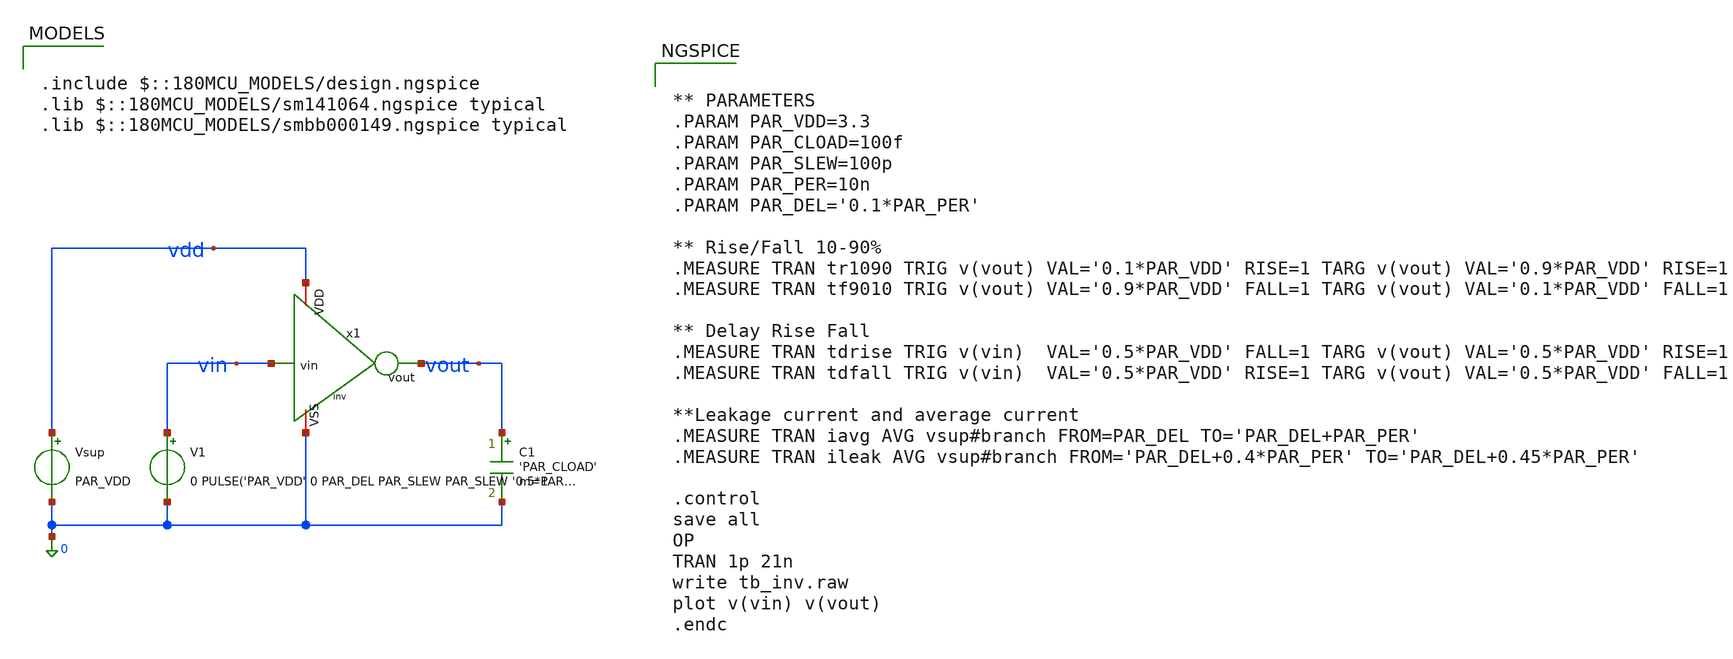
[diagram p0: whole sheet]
** sch_path: sar_logic/sar_designs/tb_inv.sch
**.subckt tb_inv
V1 vin 0 0 PULSE('PAR_VDD' 0 PAR_DEL PAR_SLEW PAR_SLEW '0.5*PAR_PER' '1.0*PAR_PER')
Vsup vdd 0 PAR_VDD
C1 vout 0 'PAR_CLOAD' m=1
x1 vdd vin vout 0 inv
**** begin user architecture code

.include $::180MCU_MODELS/design.ngspice
.lib $::180MCU_MODELS/sm141064.ngspice typical
.lib $::180MCU_MODELS/smbb000149.ngspice typical



** PARAMETERS
.PARAM PAR_VDD=3.3
.PARAM PAR_CLOAD=100f
.PARAM PAR_SLEW=100p
.PARAM PAR_PER=10n
.PARAM PAR_DEL='0.1*PAR_PER'

** Rise/Fall 10-90%
.MEASURE TRAN tr1090 TRIG v(vout) VAL='0.1*PAR_VDD' RISE=1 TARG v(vout) VAL='0.9*PAR_VDD' RISE=1
.MEASURE TRAN tf9010 TRIG v(vout) VAL='0.9*PAR_VDD' FALL=1 TARG v(vout) VAL='0.1*PAR_VDD' FALL=1

** Delay Rise Fall
.MEASURE TRAN tdrise TRIG v(vin)  VAL='0.5*PAR_VDD' FALL=1 TARG v(vout) VAL='0.5*PAR_VDD' RISE=1
.MEASURE TRAN tdfall TRIG v(vin)  VAL='0.5*PAR_VDD' RISE=1 TARG v(vout) VAL='0.5*PAR_VDD' FALL=1

**Leakage current and average current
.MEASURE TRAN iavg AVG vsup#branch FROM=PAR_DEL TO='PAR_DEL+PAR_PER'
.MEASURE TRAN ileak AVG vsup#branch FROM='PAR_DEL+0.4*PAR_PER' TO='PAR_DEL+0.45*PAR_PER'

.control
save all
OP
TRAN 1p 21n
write tb_inv.raw
plot v(vin) v(vout)
.endc



**** end user architecture code
**.ends

* expanding   symbol:  inv.sym # of pins=4
** sym_path: sar_logic/sar_designs/inv.sym
** sch_path: sar_logic/sar_designs/inv.sch
.subckt inv VDD vin vout VSS
*.ipin vin
*.opin vout
*.iopin VDD
*.iopin VSS
XM1 vout vin VDD VDD pfet_03v3 L=0.28u W=1u nf=1 ad='int((nf+1)/2) * W/nf * 0.18u' as='int((nf+2)/2) * W/nf * 0.18u'
+ pd='2*int((nf+1)/2) * (W/nf + 0.18u)' ps='2*int((nf+2)/2) * (W/nf + 0.18u)' nrd='0.18u / W' nrs='0.18u / W'
+ sa=0 sb=0 sd=0 m=1
XM2 vout vin VSS VSS nfet_03v3 L=0.28u W=0.5u nf=1 ad='int((nf+1)/2) * W/nf * 0.18u' as='int((nf+2)/2) * W/nf * 0.18u'
+ pd='2*int((nf+1)/2) * (W/nf + 0.18u)' ps='2*int((nf+2)/2) * (W/nf + 0.18u)' nrd='0.18u / W' nrs='0.18u / W'
+ sa=0 sb=0 sd=0 m=1
.ends

.end
